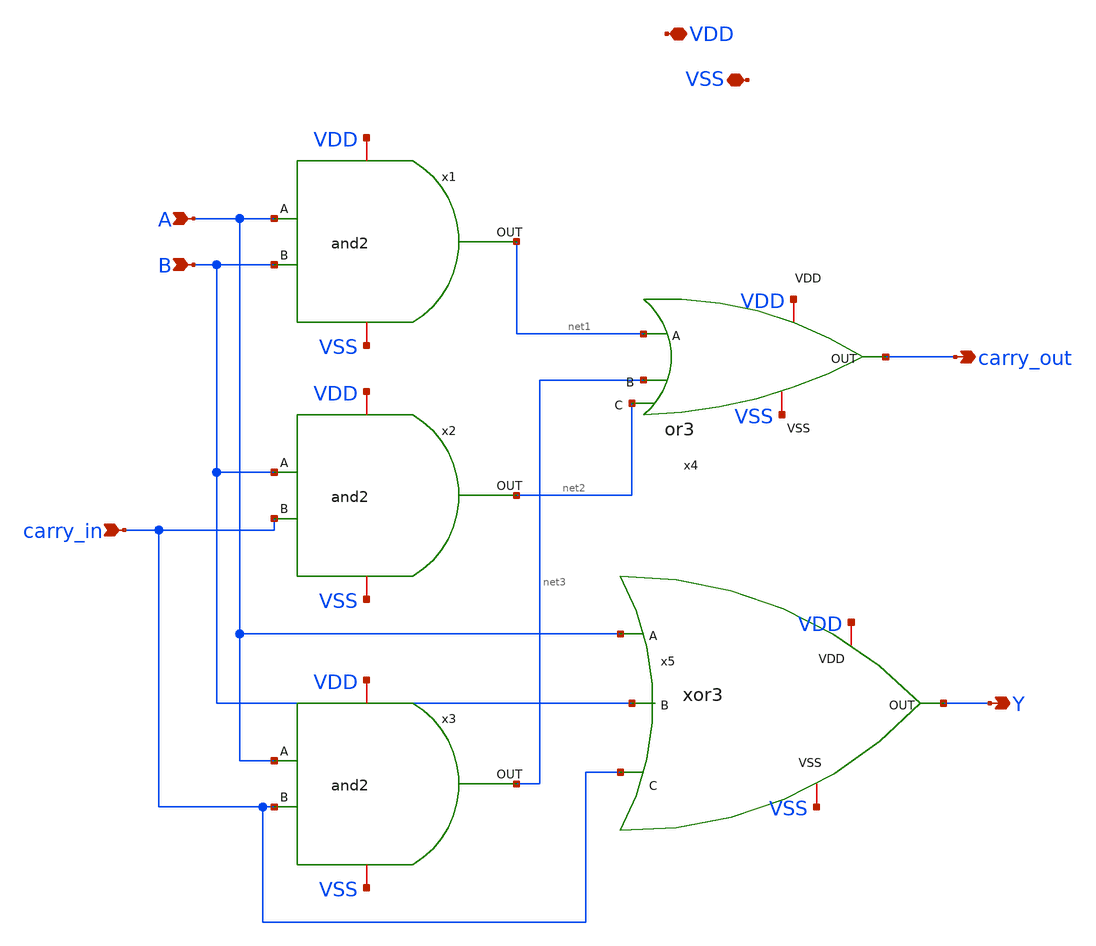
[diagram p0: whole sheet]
** sch_path: design/ARRAY_MULTIPLIER/xschem/fulladder.sch
**.subckt fulladder A B carry_in Y carry_out VDD VSS
*.ipin A
*.ipin B
*.ipin carry_in
*.opin Y
*.opin carry_out
*.iopin VDD
*.iopin VSS
x1 VSS A B VDD net1 and2
x2 VSS B carry_in VDD net2 and2
x3 VSS A carry_in VDD net3 and2
x4 VDD net1 net3 net2 carry_out VSS or3
x5 VDD A Y B carry_in VSS xor3
**.ends
.end
